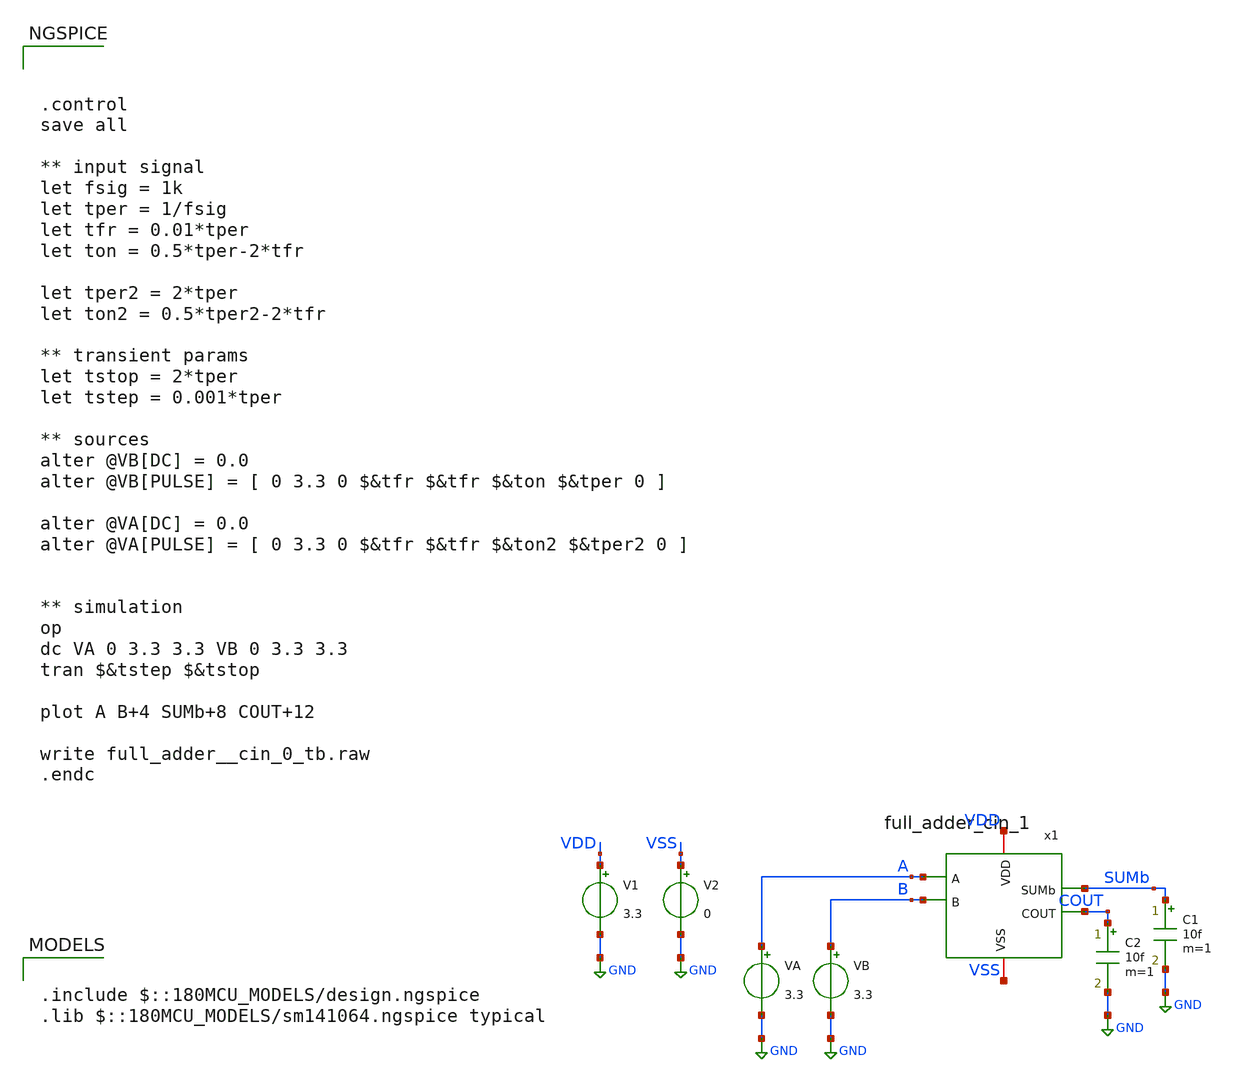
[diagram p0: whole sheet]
** sch_path: CAD4/full_adder_cin_1_tb.sch
**.subckt full_adder_cin_1_tb
V1 VDD GND 3.3
VA A GND 3.3
VB B GND 3.3
C1 SUMb GND 10f m=1
V2 VSS GND 0
C2 COUT GND 10f m=1
x1 VDD VSS A B SUMb COUT full_adder_cin_1
**** begin user architecture code

.include $::180MCU_MODELS/design.ngspice
.lib $::180MCU_MODELS/sm141064.ngspice typical




.control
save all

** input signal
let fsig = 1k
let tper = 1/fsig
let tfr = 0.01*tper
let ton = 0.5*tper-2*tfr

let tper2 = 2*tper
let ton2 = 0.5*tper2-2*tfr

** transient params
let tstop = 2*tper
let tstep = 0.001*tper

** sources
alter @VB[DC] = 0.0
alter @VB[PULSE] = [ 0 3.3 0 $&tfr $&tfr $&ton $&tper 0 ]

alter @VA[DC] = 0.0
alter @VA[PULSE] = [ 0 3.3 0 $&tfr $&tfr $&ton2 $&tper2 0 ]


** simulation
op
dc VA 0 3.3 3.3 VB 0 3.3 3.3
tran $&tstep $&tstop

plot A B+4 SUMb+8 COUT+12

write full_adder__cin_0_tb.raw
.endc


**** end user architecture code
**.ends

* expanding   symbol:  engn1600-team1/CAD4/full_adder_cin_1.sym # of pins=6
** sym_path: CAD4/full_adder_cin_1.sym
** sch_path: CAD4/full_adder_cin_1.sch
.subckt full_adder_cin_1 VDD VSS A B SUMb COUT
*.iopin VDD
*.iopin VSS
*.ipin A
*.ipin B
*.opin SUMb
*.opin COUT
XM1 net1 A VDD VDD pfet_03v3 L=0.28u W=0.22u nf=1 ad='int((nf+1)/2) * W/nf * 0.18u' as='int((nf+2)/2) * W/nf * 0.18u'
+ pd='2*int((nf+1)/2) * (W/nf + 0.18u)' ps='2*int((nf+2)/2) * (W/nf + 0.18u)' nrd='0.18u / W' nrs='0.18u / W'
+ sa=0 sb=0 sd=0 m=1
XM2 net3 B net1 VDD pfet_03v3 L=0.28u W=0.22u nf=1 ad='int((nf+1)/2) * W/nf * 0.18u' as='int((nf+2)/2) * W/nf * 0.18u'
+ pd='2*int((nf+1)/2) * (W/nf + 0.18u)' ps='2*int((nf+2)/2) * (W/nf + 0.18u)' nrd='0.18u / W' nrs='0.18u / W'
+ sa=0 sb=0 sd=0 m=1
XM7 net2 A VSS VSS nfet_03v3 L=0.28u W=0.22u nf=1 ad='int((nf+1)/2) * W/nf * 0.18u' as='int((nf+2)/2) * W/nf * 0.18u'
+ pd='2*int((nf+1)/2) * (W/nf + 0.18u)' ps='2*int((nf+2)/2) * (W/nf + 0.18u)' nrd='0.18u / W' nrs='0.18u / W'
+ sa=0 sb=0 sd=0 m=1
XM8 net3 B net2 VSS nfet_03v3 L=0.28u W=0.22u nf=1 ad='int((nf+1)/2) * W/nf * 0.18u' as='int((nf+2)/2) * W/nf * 0.18u'
+ pd='2*int((nf+1)/2) * (W/nf + 0.18u)' ps='2*int((nf+2)/2) * (W/nf + 0.18u)' nrd='0.18u / W' nrs='0.18u / W'
+ sa=0 sb=0 sd=0 m=1
XM9 net3 A VSS VSS nfet_03v3 L=0.28u W=0.22u nf=1 ad='int((nf+1)/2) * W/nf * 0.18u' as='int((nf+2)/2) * W/nf * 0.18u'
+ pd='2*int((nf+1)/2) * (W/nf + 0.18u)' ps='2*int((nf+2)/2) * (W/nf + 0.18u)' nrd='0.18u / W' nrs='0.18u / W'
+ sa=0 sb=0 sd=0 m=1
XM10 net3 B VSS VSS nfet_03v3 L=0.28u W=0.22u nf=1 ad='int((nf+1)/2) * W/nf * 0.18u' as='int((nf+2)/2) * W/nf * 0.18u'
+ pd='2*int((nf+1)/2) * (W/nf + 0.18u)' ps='2*int((nf+2)/2) * (W/nf + 0.18u)' nrd='0.18u / W' nrs='0.18u / W'
+ sa=0 sb=0 sd=0 m=1
XM11 SUMb net3 net4 VDD pfet_03v3 L=0.28u W=0.22u nf=1 ad='int((nf+1)/2) * W/nf * 0.18u' as='int((nf+2)/2) * W/nf * 0.18u'
+ pd='2*int((nf+1)/2) * (W/nf + 0.18u)' ps='2*int((nf+2)/2) * (W/nf + 0.18u)' nrd='0.18u / W' nrs='0.18u / W'
+ sa=0 sb=0 sd=0 m=1
XM12 net4 A VDD VDD pfet_03v3 L=0.28u W=0.22u nf=1 ad='int((nf+1)/2) * W/nf * 0.18u' as='int((nf+2)/2) * W/nf * 0.18u'
+ pd='2*int((nf+1)/2) * (W/nf + 0.18u)' ps='2*int((nf+2)/2) * (W/nf + 0.18u)' nrd='0.18u / W' nrs='0.18u / W'
+ sa=0 sb=0 sd=0 m=1
XM14 net4 B VDD VDD pfet_03v3 L=0.28u W=0.22u nf=1 ad='int((nf+1)/2) * W/nf * 0.18u' as='int((nf+2)/2) * W/nf * 0.18u'
+ pd='2*int((nf+1)/2) * (W/nf + 0.18u)' ps='2*int((nf+2)/2) * (W/nf + 0.18u)' nrd='0.18u / W' nrs='0.18u / W'
+ sa=0 sb=0 sd=0 m=1
XM18 SUMb net3 VSS VSS nfet_03v3 L=0.28u W=0.22u nf=1 ad='int((nf+1)/2) * W/nf * 0.18u' as='int((nf+2)/2) * W/nf * 0.18u'
+ pd='2*int((nf+1)/2) * (W/nf + 0.18u)' ps='2*int((nf+2)/2) * (W/nf + 0.18u)' nrd='0.18u / W' nrs='0.18u / W'
+ sa=0 sb=0 sd=0 m=1
XM23 SUMb B net5 VSS nfet_03v3 L=0.28u W=0.22u nf=1 ad='int((nf+1)/2) * W/nf * 0.18u' as='int((nf+2)/2) * W/nf * 0.18u'
+ pd='2*int((nf+1)/2) * (W/nf + 0.18u)' ps='2*int((nf+2)/2) * (W/nf + 0.18u)' nrd='0.18u / W' nrs='0.18u / W'
+ sa=0 sb=0 sd=0 m=1
XM24 net5 A VSS VSS nfet_03v3 L=0.28u W=0.22u nf=1 ad='int((nf+1)/2) * W/nf * 0.18u' as='int((nf+2)/2) * W/nf * 0.18u'
+ pd='2*int((nf+1)/2) * (W/nf + 0.18u)' ps='2*int((nf+2)/2) * (W/nf + 0.18u)' nrd='0.18u / W' nrs='0.18u / W'
+ sa=0 sb=0 sd=0 m=1
XM25 COUT net3 VDD VDD pfet_03v3 L=0.28u W=0.22u nf=1 ad='int((nf+1)/2) * W/nf * 0.18u' as='int((nf+2)/2) * W/nf * 0.18u'
+ pd='2*int((nf+1)/2) * (W/nf + 0.18u)' ps='2*int((nf+2)/2) * (W/nf + 0.18u)' nrd='0.18u / W' nrs='0.18u / W'
+ sa=0 sb=0 sd=0 m=1
XM26 COUT net3 VSS VSS nfet_03v3 L=0.28u W=0.22u nf=1 ad='int((nf+1)/2) * W/nf * 0.18u' as='int((nf+2)/2) * W/nf * 0.18u'
+ pd='2*int((nf+1)/2) * (W/nf + 0.18u)' ps='2*int((nf+2)/2) * (W/nf + 0.18u)' nrd='0.18u / W' nrs='0.18u / W'
+ sa=0 sb=0 sd=0 m=1
.ends

.GLOBAL GND
.end
